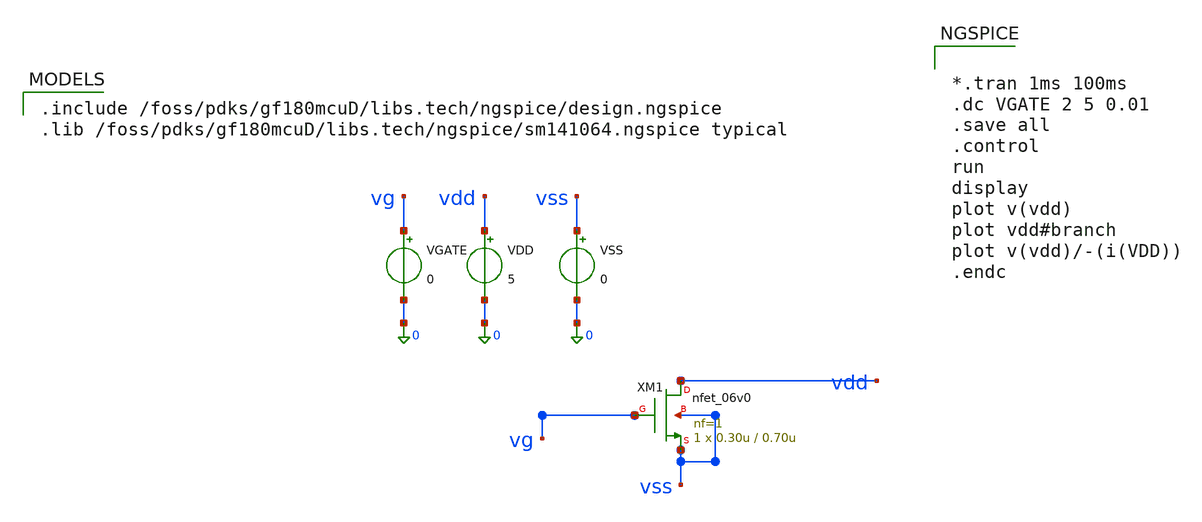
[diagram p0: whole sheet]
** sch_path: activities/opamp3An/FINAL_NMOSresistor_tb.sch
**.subckt FINAL_NMOSresistor_tb
VGATE vg 0 0
VDD vdd 0 5
VSS vss 0 0
XM1 vdd vg vss vss nfet_06v0 L=0.70u W=0.30u nf=1 ad='int((nf+1)/2) * W/nf * 0.18u' as='int((nf+2)/2) * W/nf * 0.18u'
+ pd='2*int((nf+1)/2) * (W/nf + 0.18u)' ps='2*int((nf+2)/2) * (W/nf + 0.18u)' nrd='0.18u / W' nrs='0.18u / W'
+ sa=0 sb=0 sd=0 m=1
**** begin user architecture code

.include /foss/pdks/gf180mcuD/libs.tech/ngspice/design.ngspice
.lib /foss/pdks/gf180mcuD/libs.tech/ngspice/sm141064.ngspice typical



*.tran 1ms 100ms
.dc VGATE 2 5 0.01
.save all
.control
run
display
plot v(vdd)
plot vdd#branch
plot v(vdd)/-(i(VDD))
.endc


**** end user architecture code
**.ends
.end
